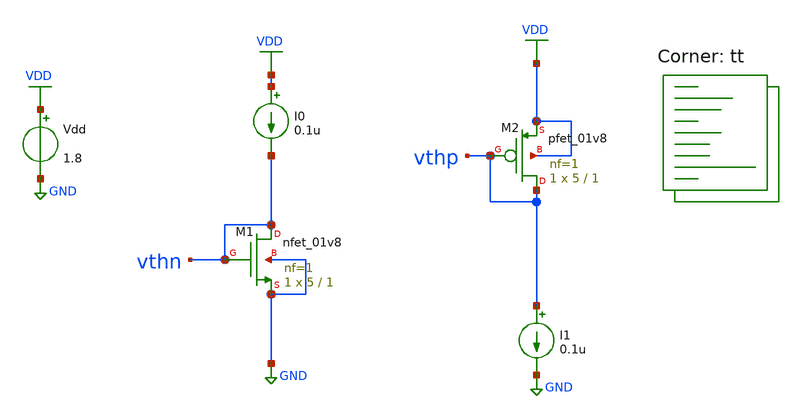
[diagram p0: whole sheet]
** sch_path: vth.sch
**.subckt vth
Vdd VDD GND 1.8
XM1 vthn vthn GND GND sky130_fd_pr__nfet_01v8 L=1 W=5 nf=1 ad='int((nf+1)/2) * W/nf * 0.29' as='int((nf+2)/2) * W/nf * 0.29'
+ pd='2*int((nf+1)/2) * (W/nf + 0.29)' ps='2*int((nf+2)/2) * (W/nf + 0.29)' nrd='0.29 / W' nrs='0.29 / W'
+ sa=0 sb=0 sd=0 mult=1 m=1
XM2 vthp vthp VDD VDD sky130_fd_pr__pfet_01v8 L=1 W=5 nf=1 ad='int((nf+1)/2) * W/nf * 0.29' as='int((nf+2)/2) * W/nf * 0.29'
+ pd='2*int((nf+1)/2) * (W/nf + 0.29)' ps='2*int((nf+2)/2) * (W/nf + 0.29)' nrd='0.29 / W' nrs='0.29 / W'
+ sa=0 sb=0 sd=0 mult=1 m=1
I0 VDD vthn 0.1u
I1 vthp GND 0.1u
**** begin user architecture code



.options savecurrents

.control
save all
tran 1n 10n

let id_nmos=@m.xm1.msky130_fd_pr__nfet_01v8[id]
let id_pmos=@m.xm2.msky130_fd_pr__pfet_01v8[id]


print v(vthn) v(vthp)
write vth.raw

set appendwrite
.endc


.lib $::SKYWATER_MODELS/sky130.lib.spice tt
**** end user architecture code
**.ends
.GLOBAL GND
.GLOBAL VDD
.end
